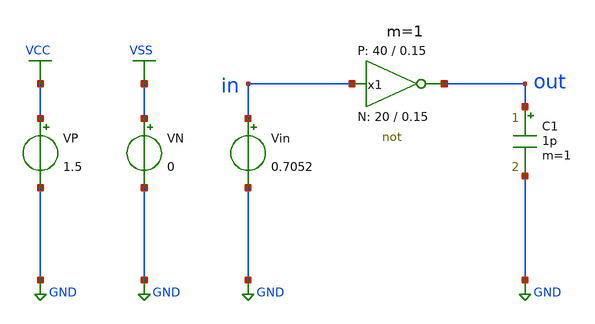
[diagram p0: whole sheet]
** sch_path: Amplifier_Inv/xschem/biasing_test.sch
* StefanSchippers/xschem_sky130/sky130_tests/not.sch:
* Copyright 2021 Stefan Frederik Schippers
* Licensed under the Apache License, Version 2.0 (the "License");
**.subckt biasing_test
x1 out in VCC VSS not W_N=20 L_N=0.15 W_P=40 L_P=0.15 m=1
VN VSS GND 0
VP VCC GND 1.5
Vin in GND 0.7052
C1 out GND 1p m=1
**** begin user architecture code

** opencircuitdesign pdks install
.lib $::SKYWATER_MODELS/sky130.lib.spice tt




.control
  op
  print @m.x1.xm1.msky130_fd_pr__nfet_01v8[gm]
  print @m.x1.xm2.msky130_fd_pr__pfet_01v8[gm]
  print @m.x1.xm1.msky130_fd_pr__nfet_01v8[gds]
  print @m.x1.xm2.msky130_fd_pr__pfet_01v8[gds]
  print @m.x1.xm1.msky130_fd_pr__nfet_01v8[cgs]
  print @m.x1.xm2.msky130_fd_pr__pfet_01v8[cgs]
  save all
  write tb_inv_sky130_op.raw
.endc


**** end user architecture code
**.ends

* expanding   symbol:  sky130_tests/not.sym # of pins=2
** sym_path: sky130_tests/not.sym
** sch_path: sky130_tests/not.sch
.subckt not y a VCCPIN VSSPIN     W_N=1 L_N=0.15 W_P=2 L_P=0.15
*.opin y
*.ipin a
XM1 DN a VSSPIN VSSPIN sky130_fd_pr__nfet_01v8 L=L_N W=W_N nf=1 ad='int((1 + 1)/2) * W_N / 1 * 0.29'
+ as='int((1 + 2)/2) * W_N / 1 * 0.29' pd='2*int((1 + 1)/2) * (W_N / 1 + 0.29)' ps='2*int((1 + 2)/2) * (W_N / 1 + 0.29)'
+ nrd='0.29 / W_N ' nrs='0.29 / W_N ' sa=0 sb=0 sd=0 mult=1 m=1
XM2 DP a VCCPIN VCCPIN sky130_fd_pr__pfet_01v8 L=L_P W=W_P nf=1 ad='int((nf+1)/2) * W/nf * 0.29' as='int((nf+2)/2) * W/nf * 0.29'
+ pd='2*int((nf+1)/2) * (W/nf + 0.29)' ps='2*int((nf+2)/2) * (W/nf + 0.29)' nrd='0.29 / W' nrs='0.29 / W'
+ sa=0 sb=0 sd=0 mult=1 m=1
Vmeas DP y 0
.save i(vmeas)
Vmeas1 y DN 0
.save i(vmeas1)
.save v(dp)
.save v(dn)
.ends

.GLOBAL GND
.GLOBAL VSS
.GLOBAL VCC
.end
